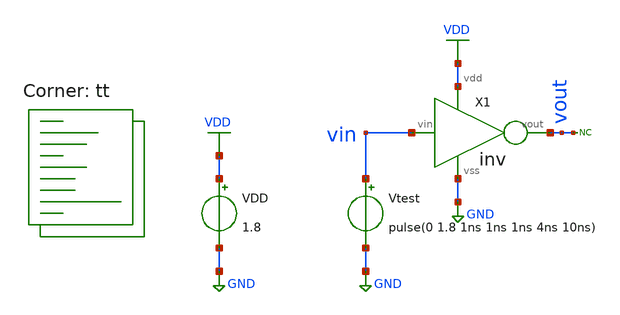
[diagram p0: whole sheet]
** sch_path: xsch/tb/tb_inv_tran.sch
**.subckt tb_inv_tran
Vtest vin GND pulse(0 1.8 1ns 1ns 1ns 4ns 10ns)
VDD VDD GND 1.8
X1 vin vout VDD GND inv
* noconn vout
**** begin user architecture code


.tran 0.01n 1u


.lib $::SKYWATER_MODELS/sky130.lib.spice tt


.save all




.param vdda=1.8


**** end user architecture code
**.ends
.GLOBAL VDD
.GLOBAL GND
.end
